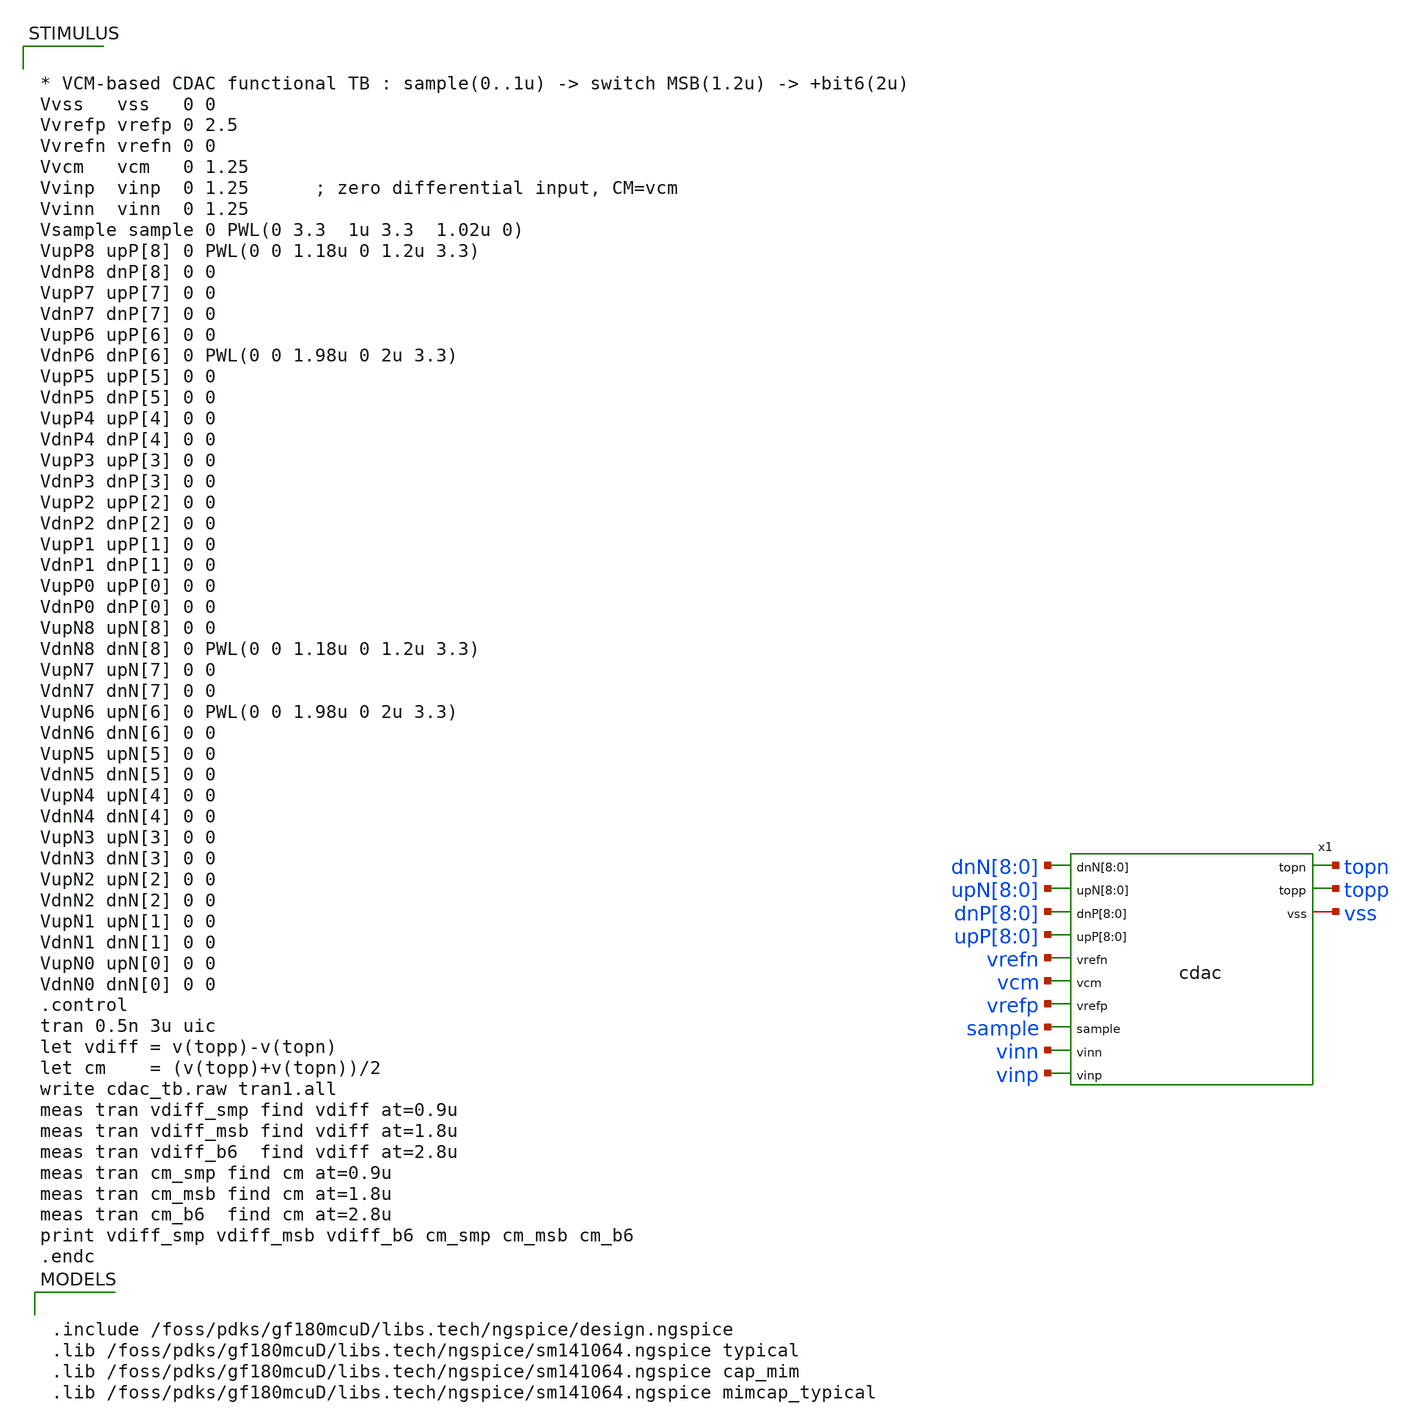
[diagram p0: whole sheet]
** sch_path: designs/libs/core_analog/saradc/tb/cdac_tb.sch
**.subckt cdac_tb
x1 dnN[8] dnN[7] dnN[6] dnN[5] dnN[4] dnN[3] dnN[2] dnN[1] dnN[0] upN[8] upN[7] upN[6] upN[5] upN[4]
+ upN[3] upN[2] upN[1] upN[0] dnP[8] dnP[7] dnP[6] dnP[5] dnP[4] dnP[3] dnP[2] dnP[1] dnP[0] upP[8] upP[7]
+ upP[6] upP[5] upP[4] upP[3] upP[2] upP[1] upP[0] topn topp vss vrefn vcm vrefp sample vinn vinp cdac
**** begin user architecture code


.include /foss/pdks/gf180mcuD/libs.tech/ngspice/design.ngspice
.lib /foss/pdks/gf180mcuD/libs.tech/ngspice/sm141064.ngspice typical
.lib /foss/pdks/gf180mcuD/libs.tech/ngspice/sm141064.ngspice cap_mim
.lib /foss/pdks/gf180mcuD/libs.tech/ngspice/sm141064.ngspice mimcap_typical




* VCM-based CDAC functional TB : sample(0..1u) -> switch MSB(1.2u) -> +bit6(2u)
Vvss   vss   0 0
Vvrefp vrefp 0 2.5
Vvrefn vrefn 0 0
Vvcm   vcm   0 1.25
Vvinp  vinp  0 1.25      ; zero differential input, CM=vcm
Vvinn  vinn  0 1.25
Vsample sample 0 PWL(0 3.3  1u 3.3  1.02u 0)
VupP8 upP[8] 0 PWL(0 0 1.18u 0 1.2u 3.3)
VdnP8 dnP[8] 0 0
VupP7 upP[7] 0 0
VdnP7 dnP[7] 0 0
VupP6 upP[6] 0 0
VdnP6 dnP[6] 0 PWL(0 0 1.98u 0 2u 3.3)
VupP5 upP[5] 0 0
VdnP5 dnP[5] 0 0
VupP4 upP[4] 0 0
VdnP4 dnP[4] 0 0
VupP3 upP[3] 0 0
VdnP3 dnP[3] 0 0
VupP2 upP[2] 0 0
VdnP2 dnP[2] 0 0
VupP1 upP[1] 0 0
VdnP1 dnP[1] 0 0
VupP0 upP[0] 0 0
VdnP0 dnP[0] 0 0
VupN8 upN[8] 0 0
VdnN8 dnN[8] 0 PWL(0 0 1.18u 0 1.2u 3.3)
VupN7 upN[7] 0 0
VdnN7 dnN[7] 0 0
VupN6 upN[6] 0 PWL(0 0 1.98u 0 2u 3.3)
VdnN6 dnN[6] 0 0
VupN5 upN[5] 0 0
VdnN5 dnN[5] 0 0
VupN4 upN[4] 0 0
VdnN4 dnN[4] 0 0
VupN3 upN[3] 0 0
VdnN3 dnN[3] 0 0
VupN2 upN[2] 0 0
VdnN2 dnN[2] 0 0
VupN1 upN[1] 0 0
VdnN1 dnN[1] 0 0
VupN0 upN[0] 0 0
VdnN0 dnN[0] 0 0
.control
tran 0.5n 3u uic
let vdiff = v(topp)-v(topn)
let cm    = (v(topp)+v(topn))/2
write cdac_tb.raw tran1.all
meas tran vdiff_smp find vdiff at=0.9u
meas tran vdiff_msb find vdiff at=1.8u
meas tran vdiff_b6  find vdiff at=2.8u
meas tran cm_smp find cm at=0.9u
meas tran cm_msb find cm at=1.8u
meas tran cm_b6  find cm at=2.8u
print vdiff_smp vdiff_msb vdiff_b6 cm_smp cm_msb cm_b6
.endc


**** end user architecture code
**.ends
.end
